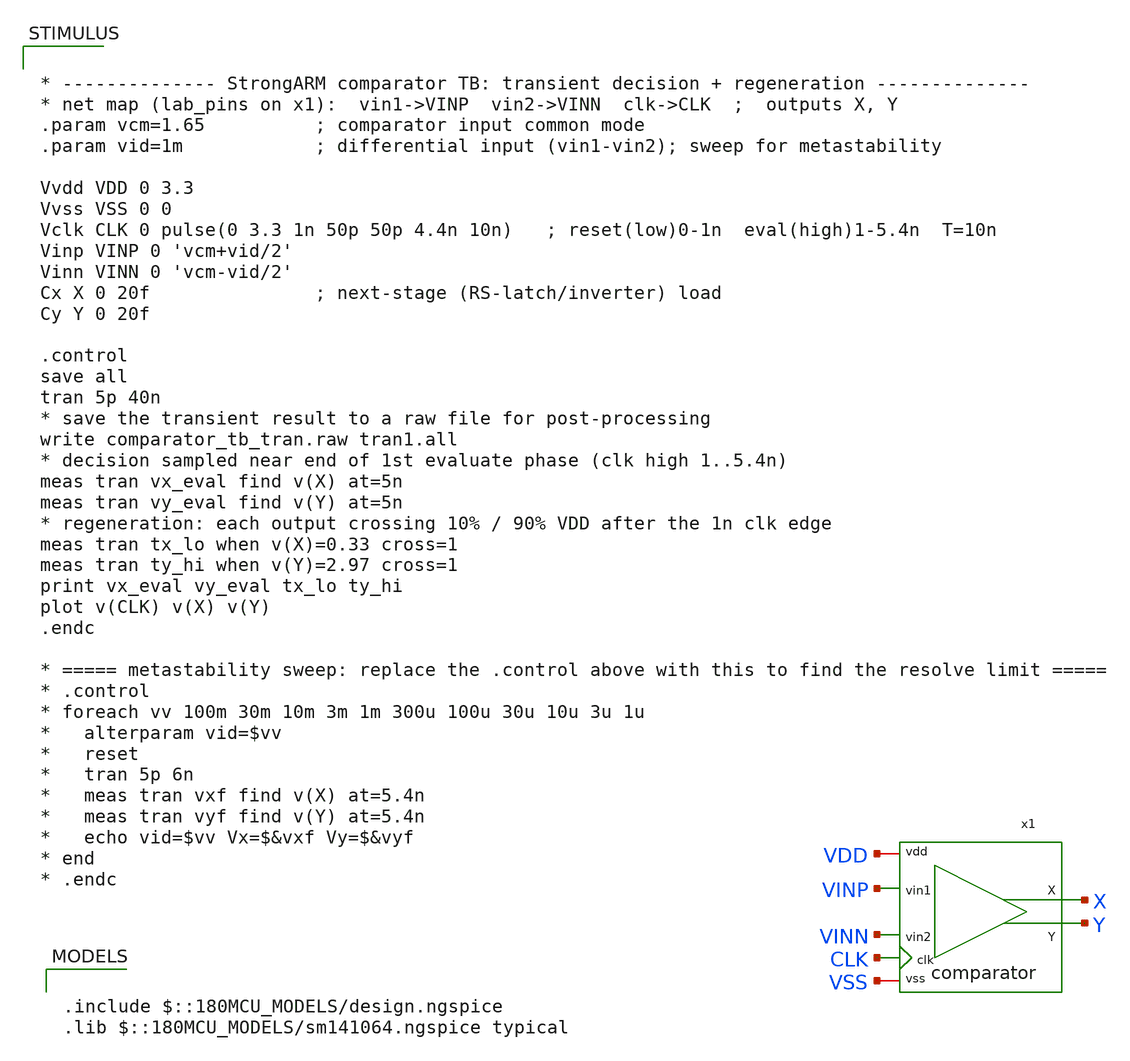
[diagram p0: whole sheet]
** sch_path: designs/libs/core_analog/saradc/tb/comparator_tb_tran.sch
**.subckt comparator_tb_tran
x1 VDD VSS X VINP Y VINN CLK comparator
**** begin user architecture code

.include $::180MCU_MODELS/design.ngspice
.lib $::180MCU_MODELS/sm141064.ngspice typical



* -------------- StrongARM comparator TB: transient decision + regeneration --------------
* net map (lab_pins on x1):  vin1->VINP  vin2->VINN  clk->CLK  ;  outputs X, Y
.param vcm=1.65          ; comparator input common mode
.param vid=1m            ; differential input (vin1-vin2); sweep for metastability

Vvdd VDD 0 3.3
Vvss VSS 0 0
Vclk CLK 0 pulse(0 3.3 1n 50p 50p 4.4n 10n)   ; reset(low)0-1n  eval(high)1-5.4n  T=10n
Vinp VINP 0 'vcm+vid/2'
Vinn VINN 0 'vcm-vid/2'
Cx X 0 20f               ; next-stage (RS-latch/inverter) load
Cy Y 0 20f

.control
save all
tran 5p 40n
* save the transient result to a raw file for post-processing
write comparator_tb_tran.raw tran1.all
* decision sampled near end of 1st evaluate phase (clk high 1..5.4n)
meas tran vx_eval find v(X) at=5n
meas tran vy_eval find v(Y) at=5n
* regeneration: each output crossing 10% / 90% VDD after the 1n clk edge
meas tran tx_lo when v(X)=0.33 cross=1
meas tran ty_hi when v(Y)=2.97 cross=1
print vx_eval vy_eval tx_lo ty_hi
plot v(CLK) v(X) v(Y)
.endc

* ===== metastability sweep: replace the .control above with this to find the resolve limit =====
* .control
* foreach vv 100m 30m 10m 3m 1m 300u 100u 30u 10u 3u 1u
*   alterparam vid=$vv
*   reset
*   tran 5p 6n
*   meas tran vxf find v(X) at=5.4n
*   meas tran vyf find v(Y) at=5.4n
*   echo vid=$vv Vx=$&vxf Vy=$&vyf
* end
* .endc


**** end user architecture code
**.ends

* expanding   symbol:  comparator.sym # of pins=7
** sym_path: designs/libs/core_analog/saradc/comparator.sym
** sch_path: designs/libs/core_analog/saradc/comparator.sch
.subckt comparator vdd vss X vin1 Y vin2 clk
*.iopin vdd
*.iopin vss
*.ipin vin1
*.ipin vin2
*.ipin clk
*.opin X
*.opin Y
XM1 P vin1 net1 vss nfet_03v3 L=0.5u W=4u nf=4 ad='int((nf+1)/2) * W/nf * 0.18u' as='int((nf+2)/2) * W/nf * 0.18u'
+ pd='2*int((nf+1)/2) * (W/nf + 0.18u)' ps='2*int((nf+2)/2) * (W/nf + 0.18u)' nrd='0.18u / W' nrs='0.18u / W'
+ sa=0 sb=0 sd=0 m=1
XM2 Q vin2 net1 vss nfet_03v3 L=0.5u W=4u nf=4 ad='int((nf+1)/2) * W/nf * 0.18u' as='int((nf+2)/2) * W/nf * 0.18u'
+ pd='2*int((nf+1)/2) * (W/nf + 0.18u)' ps='2*int((nf+2)/2) * (W/nf + 0.18u)' nrd='0.18u / W' nrs='0.18u / W'
+ sa=0 sb=0 sd=0 m=1
XM3 X Y P vss nfet_03v3 L=0.28u W=2u nf=2 ad='int((nf+1)/2) * W/nf * 0.18u' as='int((nf+2)/2) * W/nf * 0.18u'
+ pd='2*int((nf+1)/2) * (W/nf + 0.18u)' ps='2*int((nf+2)/2) * (W/nf + 0.18u)' nrd='0.18u / W' nrs='0.18u / W'
+ sa=0 sb=0 sd=0 m=1
XM4 Y X Q vss nfet_03v3 L=0.28u W=2u nf=2 ad='int((nf+1)/2) * W/nf * 0.18u' as='int((nf+2)/2) * W/nf * 0.18u'
+ pd='2*int((nf+1)/2) * (W/nf + 0.18u)' ps='2*int((nf+2)/2) * (W/nf + 0.18u)' nrd='0.18u / W' nrs='0.18u / W'
+ sa=0 sb=0 sd=0 m=1
XM5 X Y vdd vdd pfet_03v3 L=0.28u W=6u nf=2 ad='int((nf+1)/2) * W/nf * 0.18u' as='int((nf+2)/2) * W/nf * 0.18u'
+ pd='2*int((nf+1)/2) * (W/nf + 0.18u)' ps='2*int((nf+2)/2) * (W/nf + 0.18u)' nrd='0.18u / W' nrs='0.18u / W'
+ sa=0 sb=0 sd=0 m=1
XM6 Y X vdd vdd pfet_03v3 L=0.28u W=6u nf=2 ad='int((nf+1)/2) * W/nf * 0.18u' as='int((nf+2)/2) * W/nf * 0.18u'
+ pd='2*int((nf+1)/2) * (W/nf + 0.18u)' ps='2*int((nf+2)/2) * (W/nf + 0.18u)' nrd='0.18u / W' nrs='0.18u / W'
+ sa=0 sb=0 sd=0 m=1
XM7 net1 clk vss vss nfet_03v3 L=0.28u W=6u nf=4 ad='int((nf+1)/2) * W/nf * 0.18u' as='int((nf+2)/2) * W/nf * 0.18u'
+ pd='2*int((nf+1)/2) * (W/nf + 0.18u)' ps='2*int((nf+2)/2) * (W/nf + 0.18u)' nrd='0.18u / W' nrs='0.18u / W'
+ sa=0 sb=0 sd=0 m=1
XM8 X clk vdd vdd pfet_03v3 L=0.28u W=2u nf=1 ad='int((nf+1)/2) * W/nf * 0.18u' as='int((nf+2)/2) * W/nf * 0.18u'
+ pd='2*int((nf+1)/2) * (W/nf + 0.18u)' ps='2*int((nf+2)/2) * (W/nf + 0.18u)' nrd='0.18u / W' nrs='0.18u / W'
+ sa=0 sb=0 sd=0 m=1
XM9 P clk vdd vdd pfet_03v3 L=0.28u W=2u nf=1 ad='int((nf+1)/2) * W/nf * 0.18u' as='int((nf+2)/2) * W/nf * 0.18u'
+ pd='2*int((nf+1)/2) * (W/nf + 0.18u)' ps='2*int((nf+2)/2) * (W/nf + 0.18u)' nrd='0.18u / W' nrs='0.18u / W'
+ sa=0 sb=0 sd=0 m=1
XM10 Y clk vdd vdd pfet_03v3 L=0.28u W=2u nf=1 ad='int((nf+1)/2) * W/nf * 0.18u' as='int((nf+2)/2) * W/nf * 0.18u'
+ pd='2*int((nf+1)/2) * (W/nf + 0.18u)' ps='2*int((nf+2)/2) * (W/nf + 0.18u)' nrd='0.18u / W' nrs='0.18u / W'
+ sa=0 sb=0 sd=0 m=1
XM11 Q clk vdd vdd pfet_03v3 L=0.28u W=2u nf=1 ad='int((nf+1)/2) * W/nf * 0.18u' as='int((nf+2)/2) * W/nf * 0.18u'
+ pd='2*int((nf+1)/2) * (W/nf + 0.18u)' ps='2*int((nf+2)/2) * (W/nf + 0.18u)' nrd='0.18u / W' nrs='0.18u / W'
+ sa=0 sb=0 sd=0 m=1
.ends

.end
